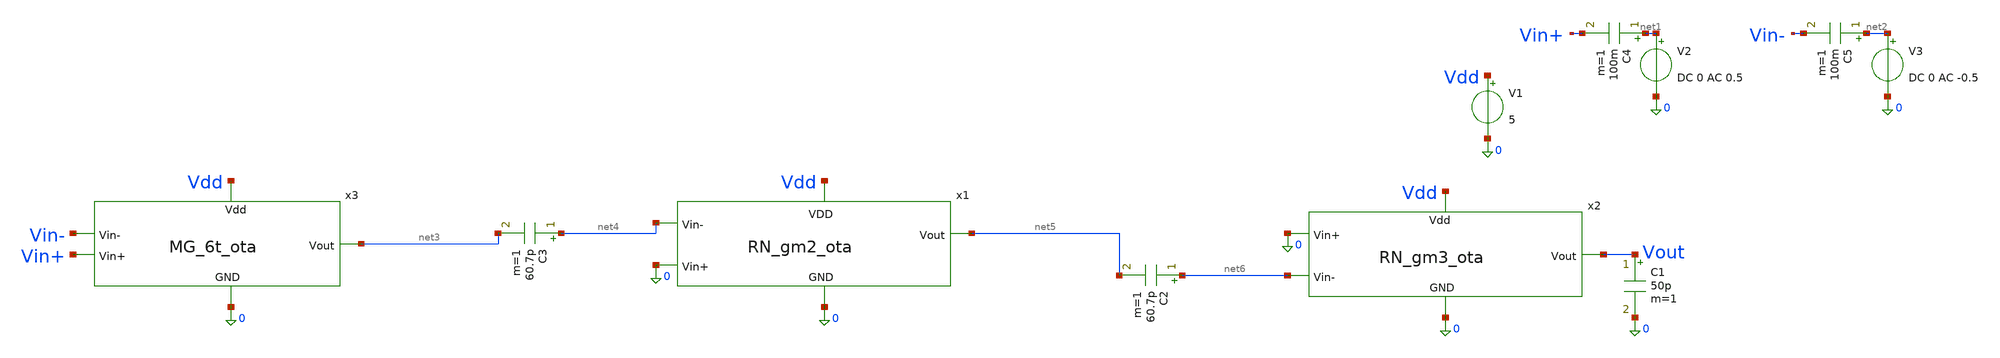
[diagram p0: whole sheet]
** sch_path: MRTMOS_final_chip/final_tb.sch
**.subckt final_tb
C1 Vout 0 50p m=1
V1 Vdd 0 5
V2 net1 0 DC 0 AC 0.5
V3 net2 0 DC 0 AC -0.5
x1 Vdd net5 net4 0 0 RN_gm2_ota
x2 Vdd Vout 0 net6 0 RN_gm3_ota
x3 Vdd net3 Vin- Vin+ 0 MG_6t_ota
C2 net6 net5 60.7p m=1
C3 net4 net3 60.7p m=1
C4 net1 Vin+ 100m m=1
C5 net2 Vin- 100m m=1
**** begin user architecture code


.include /foss/pdks/gf180mcuD/libs.tech/ngspice/design.ngspice
.lib /foss/pdks/gf180mcuD/libs.tech/ngspice/sm141064.ngspice typical
.lib /foss/pdks/gf180mcuD/libs.tech/ngspice/sm141064.ngspice res_typical
.lib /foss/pdks/gf180mcuD/libs.tech/ngspice/sm141064.ngspice moscap_typical
.lib /foss/pdks/gf180mcuD/libs.tech/ngspice/sm141064.ngspice mimcap_typical
.lib /foss/pdks/gf180mcuD/libs.tech/ngspice/sm141064.ngspice cap_mim




* AC & Transient Step Stimulus
* - DC bias: 3.0V
* - AC magnitude: 1V (for Bode plot)
* - Pulse: 2.95V to 3.05V step (100mV step), 5ns edges, 1MHz frequency (0.5us width, 1us period)


* --- 2. Simulation Control Block ---
.control
  save all

  * A. DC Operating Point Analysis
  op
  print v(Vout) v(Vin+) v(Vin-)

  * B. AC Sweep (Bode Plot: Gain & Phase)
  ac dec 20 1 100Meg
  set units = degrees
  plot vdb(Vout) vs frequency title 'Open-Loop AC Gain (dB)'
  plot cph(Vout) vs frequency title 'Open-Loop AC Phase (Degrees)'

  * C. Transient Analysis (1 MHz Step Response)
  * Run for 5 microseconds (5 complete 1MHz cycles) with a 1ns step
*  alter @v2[pulse] = [ 2.9 3.1 0 5n 5n 0.495u 1u ]
*  tran 1n 5u
*  plot v(Vin+) v(Vin-) v(Vout) title '1MHz Transient Step Response'

  * Save the raw data
  write RN_gm3_ota_sim.raw
.endc

.options savecurrents


**** end user architecture code
**.ends
.end
